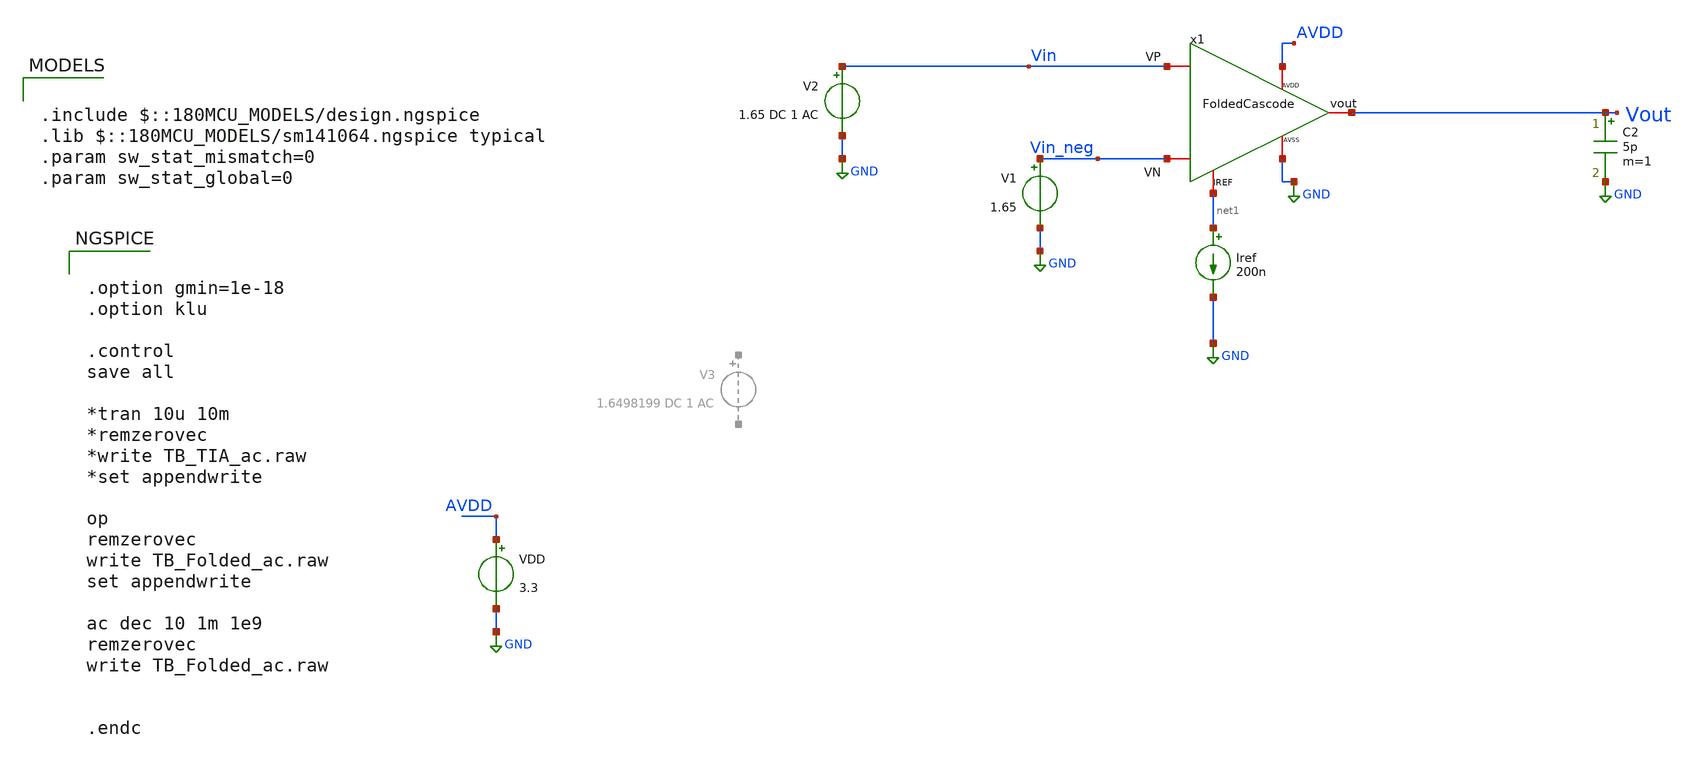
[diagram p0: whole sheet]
** sch_path: Voltage_Reference/LDO/Folded/TB_Folded_ac.sch
**.subckt TB_Folded_ac
VDD AVDD GND 3.3
Iref net1 GND 200n
V1 Vin_neg GND 1.65
C2 Vout GND 5p m=1
V2 Vin GND 1.65 DC 1 AC
x1 Vin Vin_neg Vout net1 AVDD GND FoldedCascode
**** begin user architecture code

.include $::180MCU_MODELS/design.ngspice
.lib $::180MCU_MODELS/sm141064.ngspice typical
.param sw_stat_mismatch=0
.param sw_stat_global=0



.option gmin=1e-18
.option klu

.control
save all

*tran 10u 10m
*remzerovec
*write TB_TIA_ac.raw
*set appendwrite

op
remzerovec
write TB_Folded_ac.raw
set appendwrite

ac dec 10 1m 1e9
remzerovec
write TB_Folded_ac.raw


.endc


**** end user architecture code
**.ends
.GLOBAL GND
.end
